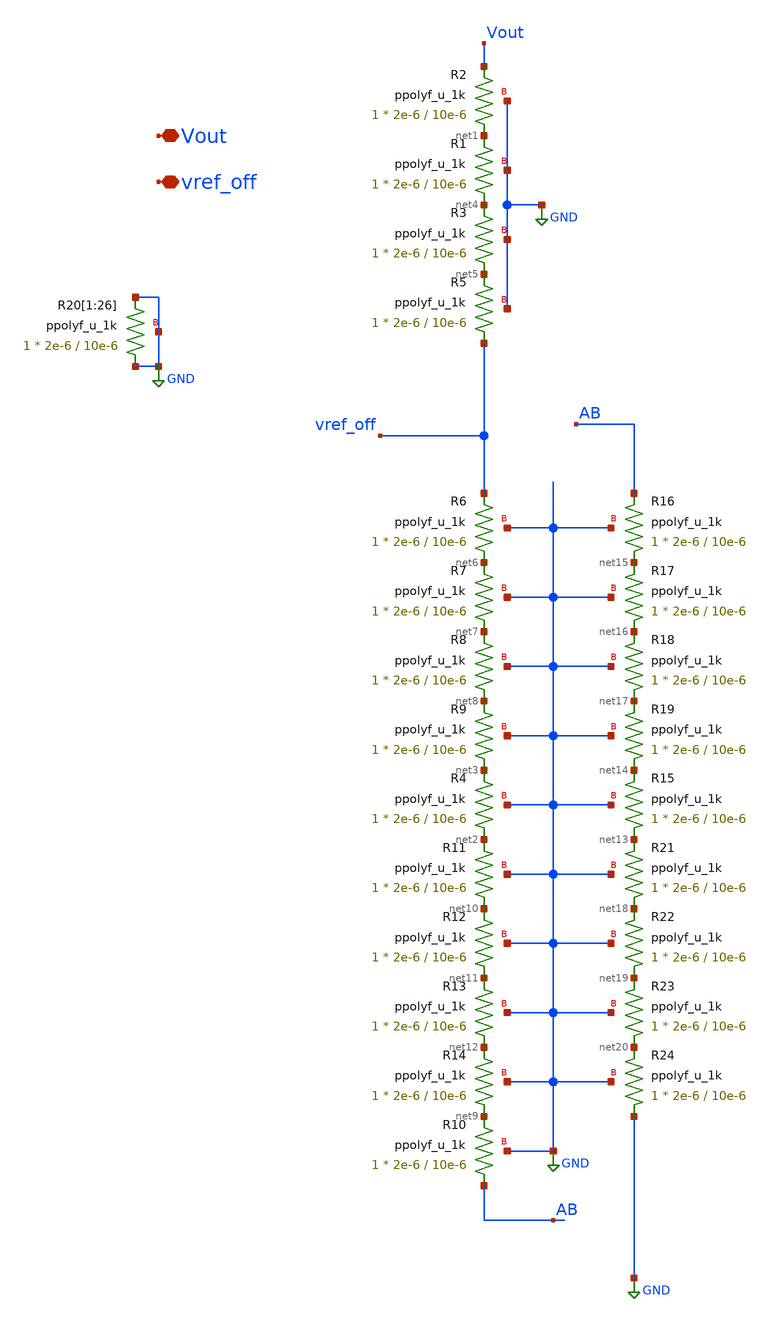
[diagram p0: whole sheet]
** sch_path: Voltage_Reference/LDO/Res_Div.sch
**.subckt Res_Div Vout vref_off
*.iopin Vout
*.iopin vref_off
XR2 net1 Vout GND ppolyf_u_1k r_width=2e-6 r_length=10e-6 m=1
XR4 net2 net3 GND ppolyf_u_1k r_width=2e-6 r_length=10e-6 m=1
XR1 net4 net1 GND ppolyf_u_1k r_width=2e-6 r_length=10e-6 m=1
XR3 net5 net4 GND ppolyf_u_1k r_width=2e-6 r_length=10e-6 m=1
XR5 vref_off net5 GND ppolyf_u_1k r_width=2e-6 r_length=10e-6 m=1
XR6 net6 vref_off GND ppolyf_u_1k r_width=2e-6 r_length=10e-6 m=1
XR7 net7 net6 GND ppolyf_u_1k r_width=2e-6 r_length=10e-6 m=1
XR8 net8 net7 GND ppolyf_u_1k r_width=2e-6 r_length=10e-6 m=1
XR9 net3 net8 GND ppolyf_u_1k r_width=2e-6 r_length=10e-6 m=1
XR10 AB net9 GND ppolyf_u_1k r_width=2e-6 r_length=10e-6 m=1
XR11 net10 net2 GND ppolyf_u_1k r_width=2e-6 r_length=10e-6 m=1
XR12 net11 net10 GND ppolyf_u_1k r_width=2e-6 r_length=10e-6 m=1
XR13 net12 net11 GND ppolyf_u_1k r_width=2e-6 r_length=10e-6 m=1
XR14 net9 net12 GND ppolyf_u_1k r_width=2e-6 r_length=10e-6 m=1
XR15 net13 net14 GND ppolyf_u_1k r_width=2e-6 r_length=10e-6 m=1
XR16 net15 AB GND ppolyf_u_1k r_width=2e-6 r_length=10e-6 m=1
XR17 net16 net15 GND ppolyf_u_1k r_width=2e-6 r_length=10e-6 m=1
XR18 net17 net16 GND ppolyf_u_1k r_width=2e-6 r_length=10e-6 m=1
XR19 net14 net17 GND ppolyf_u_1k r_width=2e-6 r_length=10e-6 m=1
XR21 net18 net13 GND ppolyf_u_1k r_width=2e-6 r_length=10e-6 m=1
XR22 net19 net18 GND ppolyf_u_1k r_width=2e-6 r_length=10e-6 m=1
XR23 net20 net19 GND ppolyf_u_1k r_width=2e-6 r_length=10e-6 m=1
XR24 GND net20 GND ppolyf_u_1k r_width=2e-6 r_length=10e-6 m=1
XR20[1] GND GND GND ppolyf_u_1k r_width=2e-6 r_length=10e-6 m=1
XR20[2] GND GND GND ppolyf_u_1k r_width=2e-6 r_length=10e-6 m=1
XR20[3] GND GND GND ppolyf_u_1k r_width=2e-6 r_length=10e-6 m=1
XR20[4] GND GND GND ppolyf_u_1k r_width=2e-6 r_length=10e-6 m=1
XR20[5] GND GND GND ppolyf_u_1k r_width=2e-6 r_length=10e-6 m=1
XR20[6] GND GND GND ppolyf_u_1k r_width=2e-6 r_length=10e-6 m=1
XR20[7] GND GND GND ppolyf_u_1k r_width=2e-6 r_length=10e-6 m=1
XR20[8] GND GND GND ppolyf_u_1k r_width=2e-6 r_length=10e-6 m=1
XR20[9] GND GND GND ppolyf_u_1k r_width=2e-6 r_length=10e-6 m=1
XR20[10] GND GND GND ppolyf_u_1k r_width=2e-6 r_length=10e-6 m=1
XR20[11] GND GND GND ppolyf_u_1k r_width=2e-6 r_length=10e-6 m=1
XR20[12] GND GND GND ppolyf_u_1k r_width=2e-6 r_length=10e-6 m=1
XR20[13] GND GND GND ppolyf_u_1k r_width=2e-6 r_length=10e-6 m=1
XR20[14] GND GND GND ppolyf_u_1k r_width=2e-6 r_length=10e-6 m=1
XR20[15] GND GND GND ppolyf_u_1k r_width=2e-6 r_length=10e-6 m=1
XR20[16] GND GND GND ppolyf_u_1k r_width=2e-6 r_length=10e-6 m=1
XR20[17] GND GND GND ppolyf_u_1k r_width=2e-6 r_length=10e-6 m=1
XR20[18] GND GND GND ppolyf_u_1k r_width=2e-6 r_length=10e-6 m=1
XR20[19] GND GND GND ppolyf_u_1k r_width=2e-6 r_length=10e-6 m=1
XR20[20] GND GND GND ppolyf_u_1k r_width=2e-6 r_length=10e-6 m=1
XR20[21] GND GND GND ppolyf_u_1k r_width=2e-6 r_length=10e-6 m=1
XR20[22] GND GND GND ppolyf_u_1k r_width=2e-6 r_length=10e-6 m=1
XR20[23] GND GND GND ppolyf_u_1k r_width=2e-6 r_length=10e-6 m=1
XR20[24] GND GND GND ppolyf_u_1k r_width=2e-6 r_length=10e-6 m=1
XR20[25] GND GND GND ppolyf_u_1k r_width=2e-6 r_length=10e-6 m=1
XR20[26] GND GND GND ppolyf_u_1k r_width=2e-6 r_length=10e-6 m=1
**.ends
.GLOBAL GND
.end
